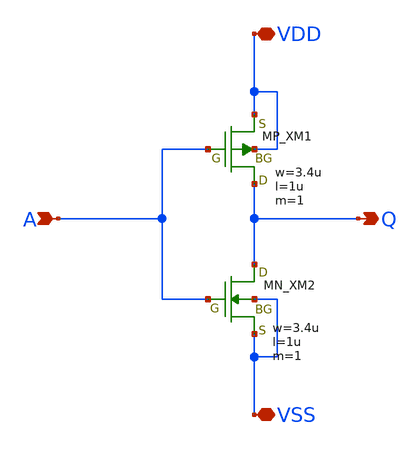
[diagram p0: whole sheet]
** sch_path: member_project/inverter/RISE-A/makoto_5555/inverter.sch
**.subckt inverter A Q VDD VSS
*.ipin A
*.opin Q
*.iopin VDD
*.iopin VSS
XXM1 Q A VDD VDD PMOS w=3.4u l=1u nrd=0 nrs=0 m=1
XXM2 Q A VSS VSS NMOS w=3.4u l=1u nrd=0 nrs=0 m=1
**.ends
.end
